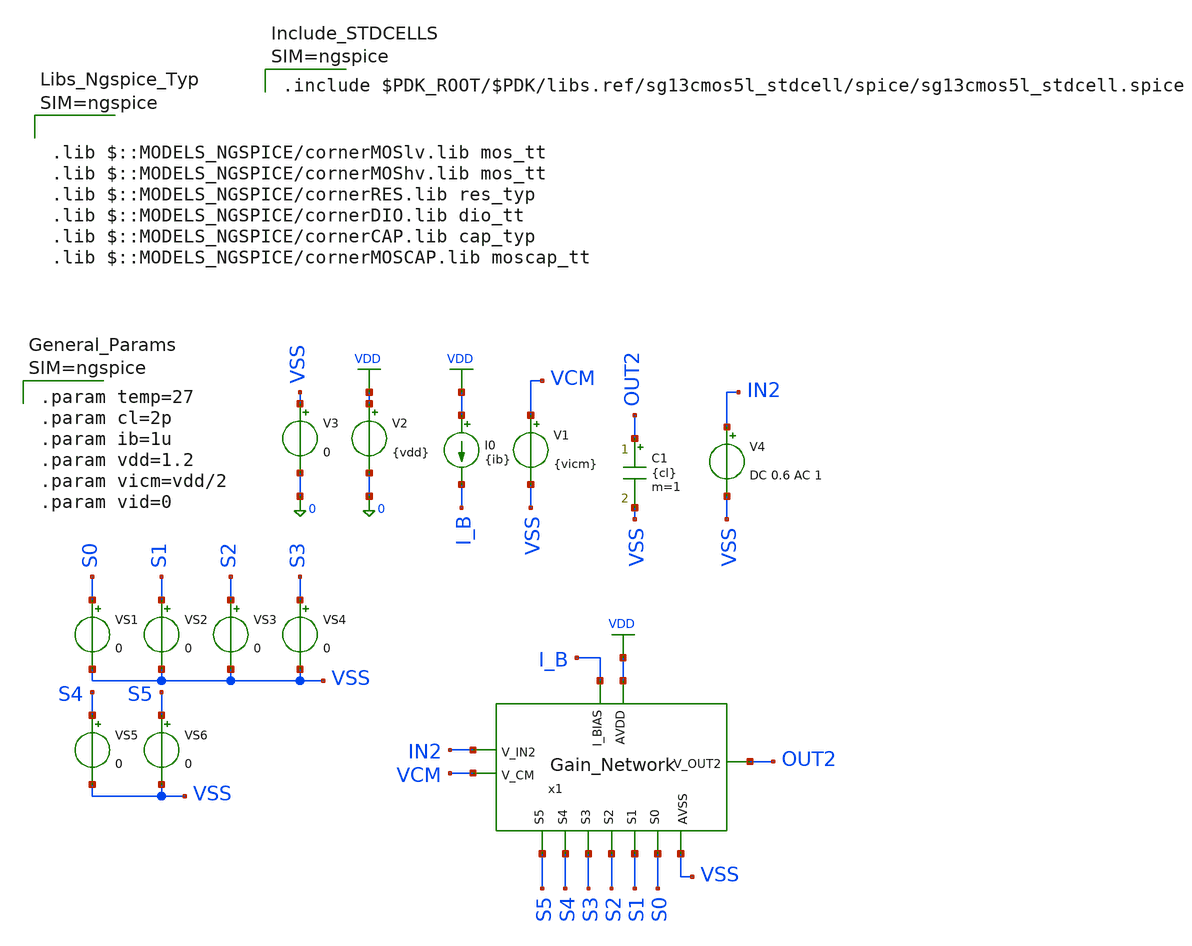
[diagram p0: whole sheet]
** sch_path: xschem/gain_network/tb/tb_gain_network/tb_gain_network.sch
**.subckt tb_gain_network
I0 VDD I_B {ib}
V2 VDD 0 {vdd}
V3 VSS 0 0
V1 VCM VSS {vicm}
C1 OUT2 VSS {cl} m=1
VS1 S0 VSS 0
VS2 S1 VSS 0
VS3 S2 VSS 0
VS4 S3 VSS 0
VS5 S4 VSS 0
VS6 S5 VSS 0
V4 IN2 VSS DC 0.6 AC 1
x1 S4 S5 S0 S2 S1 S3 VDD VCM IN2 OUT2 I_B VSS gain_network
**** begin user architecture code


.param temp=27
.param cl=2p
.param ib=1u
.param vdd=1.2
.param vicm=vdd/2
.param vid=0






.lib $::MODELS_NGSPICE/cornerMOSlv.lib mos_tt
.lib $::MODELS_NGSPICE/cornerMOShv.lib mos_tt
.lib $::MODELS_NGSPICE/cornerRES.lib res_typ
.lib $::MODELS_NGSPICE/cornerDIO.lib dio_tt
.lib $::MODELS_NGSPICE/cornerCAP.lib cap_typ
.lib $::MODELS_NGSPICE/cornerMOSCAP.lib moscap_tt





* ==============================================================================
* BINARY GAIN-STAGE NETWORK (PGA) 6-TAP AC & DC TELEMETRY CHARACTERIZATION
* Topology  : Inverting Switched-Resistor Feedback Ladder (R to 32R)
* Step Size : Pure Binary Stepping (+6.0206 dB / 2x Gain per Step)
* Technology: IHP SG13CMOS5L (130nm BiCMOS)
* ==============================================================================

.control
destroy all
save all
shell mkdir -p result
shell rm -f ./result/tb_gain_network_summary.txt

* Initialize summary report table header
echo
+ "==================================================================================================================================" >> ./result/tb_gain_network_summary.txt
echo " Tap   Code   Target(dB)   Meas(dB)   Err(dB)    Err(Step)   Acc_FS(%)   -3dB BW(kHz)
+   Vos_out(mV)   V_vg_err(mV)   P_dc(uW) " >> ./result/tb_gain_network_summary.txt
echo
+ "==================================================================================================================================" >> ./result/tb_gain_network_summary.txt

echo
+ "=================================================================================================================================="
echo " STARTING BINARY GAIN-STAGE AC & DC CHARACTERIZATION (R TO 32R, S0 TO S5)
+                                                        "
echo
+ "=================================================================================================================================="

* ------------------------------------------------------------------------------
* STEP 0: DC OFFSET PRE-CALIBRATION (NOMINAL TAP S0 AT 0 dB)
* ------------------------------------------------------------------------------
alter @vs1[dc] = 1.2
alter @vs2[dc] = 0
alter @vs3[dc] = 0
alter @vs4[dc] = 0
alter @vs5[dc] = 0
alter @vs6[dc] = 0

op
let v_vg_nominal = v(x1.net7)
echo " Calibrated Input DC Bias to Virtual Ground: " $&v_vg_nominal " V"

alter @v4[dc] = $&v_vg_nominal

set appendwrite

* ------------------------------------------------------------------------------
* STEP 1: SEQUENTIAL 6-TAP BINARY EVALUATION LOOP (S0 TO S5)
* ------------------------------------------------------------------------------
foreach tap 0 1 2 3 4 5

  * 1. Reset all 6 control switch gate voltages to 0V (OFF state)
  alter @vs1[dc] = 0
  alter @vs2[dc] = 0
  alter @vs3[dc] = 0
  alter @vs4[dc] = 0
  alter @vs5[dc] = 0
  alter @vs6[dc] = 0

  * 2. Assert active binary tap
  if ($tap = 0)
    alter @vs1[dc] = 1.2
  end
  if ($tap = 1)
    alter @vs2[dc] = 1.2
  end
  if ($tap = 2)
    alter @vs3[dc] = 1.2
  end
  if ($tap = 3)
    alter @vs4[dc] = 1.2
  end
  if ($tap = 4)
    alter @vs5[dc] = 1.2
  end
  if ($tap = 5)
    alter @vs6[dc] = 1.2
  end

  * 3. DC Operating Point Analysis
  op
  let cur_vos_mv = (v(out2) - v(vcm)) * 1e3
  let cur_vvg_mv = (v(x1.net7) - v(vcm)) * 1e3
  let cur_pdc_uw = -i(v2) * 1.2 * 1e6

  * Lock DC variables to shell environment BEFORE plot context switches to AC
  set s_vos = "$&cur_vos_mv"
  set s_vvg = "$&cur_vvg_mv"
  set s_pdc = "$&cur_pdc_uw"

  * 4. Small-Signal AC Frequency Response Analysis
  ac dec 30 10 100MEG

  let gain_db = db(v(out2))
  let ph_deg  = cph(v(out2)) * 180 / pi

  * Measure midband flatband gain at 1 kHz
  meas ac g_meas_db find gain_db at=1k

  * Measure -3 dB cutoff bandwidth
  let target_3db = g_meas_db - 3
  meas ac f_3db when gain_db=target_3db
  let f_3db_khz = f_3db / 1e3

  * 5. Binary Gain Metrics & dB-Based Error Computation
  let ideal_lin = 2^($tap)
  let ideal_db  = db(ideal_lin)
  let err_db    = g_meas_db - ideal_db
  let err_step  = err_db / 6.0206
  let acc_fs    = 100 - (abs(err_db) / 30.103 * 100)

  * Save curves into consolidated multi-run rawfile
  write ./result/tb_gain_network_all_taps.raw gain_db ph_deg

  * Lock remaining AC variables to shell environment
  set s_ideal = "$&ideal_db"
  set s_meas  = "$&g_meas_db"
  set s_err   = "$&err_db"
  set s_step  = "$&err_step"
  set s_acc   = "$&acc_fs"
  set s_f3db  = "$&f_3db_khz"

  * Print progress to terminal
  echo " S$tap | Target: $s_ideal dB | Meas: $s_meas dB | Err: $s_err dB ($s_step LSB) | BW: $s_f3db
+ kHz | Vos: $s_vos mV"

  * Append telemetry row to text report
  echo " S$tap   | $tap    | $s_ideal       | $s_meas       | $s_err     | $s_step     | $s_acc    |
+ $s_f3db        | $s_vos       | $s_vvg       | $s_pdc" >> ./result/tb_gain_network_summary.txt

end

unset appendwrite
echo
+ "=================================================================================================================================="
echo " CHARACTERIZATION COMPLETED! Full telemetry log is exported to:
+                                                                 "
echo " ./result/tb_gain_network_summary.txt
+                                                                                             "
echo " Frequency response waveforms saved to: ./result/tb_gain_network_all_taps.raw
+                                                     "
echo
+ "=================================================================================================================================="
.endc




.include $PDK_ROOT/$PDK/libs.ref/sg13cmos5l_stdcell/spice/sg13cmos5l_stdcell.spice



**** end user architecture code
**.ends
.GLOBAL VDD
.end
